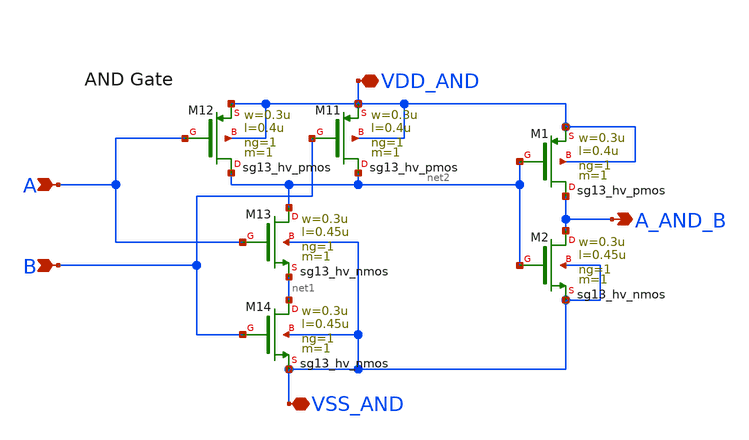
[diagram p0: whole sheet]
** sch_path: circuit_files/xschem_symbols/simp_AND.sch
**.subckt simp_AND A_AND_B A B VDD_AND VSS_AND
*.opin A_AND_B
*.ipin A
*.ipin B
*.iopin VDD_AND
*.iopin VSS_AND
XM11 net2 B VDD_AND VDD_AND sg13_hv_pmos w=0.3u l=0.4u ng=1 m=1 mm_ok=1
XM12 net2 A VDD_AND VDD_AND sg13_hv_pmos w=0.3u l=0.4u ng=1 m=1 mm_ok=1
XM13 net2 A net1 VSS_AND sg13_hv_nmos w=0.3u l=0.45u ng=1 m=1 mm_ok=1
XM14 net1 B VSS_AND VSS_AND sg13_hv_nmos w=0.3u l=0.45u ng=1 m=1 mm_ok=1
XM1 A_AND_B net2 VDD_AND VDD_AND sg13_hv_pmos w=0.3u l=0.4u ng=1 m=1 mm_ok=1
XM2 A_AND_B net2 VSS_AND VSS_AND sg13_hv_nmos w=0.3u l=0.45u ng=1 m=1 mm_ok=1
**.ends
.end
